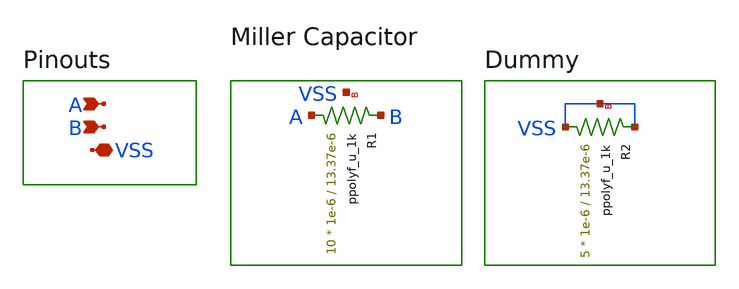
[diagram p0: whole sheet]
** sch_path: designs/libs/core_single_ended_ota/nulling_res/nulling_res.sch
**.subckt nulling_res VSS A B
*.iopin VSS
*.ipin A
*.ipin B
XR1 A B VSS ppolyf_u_1k r_width=1e-6 r_length=13.37e-6 m=10
XR2 VSS VSS VSS ppolyf_u_1k r_width=1e-6 r_length=13.37e-6 m=5
**.ends
.end
